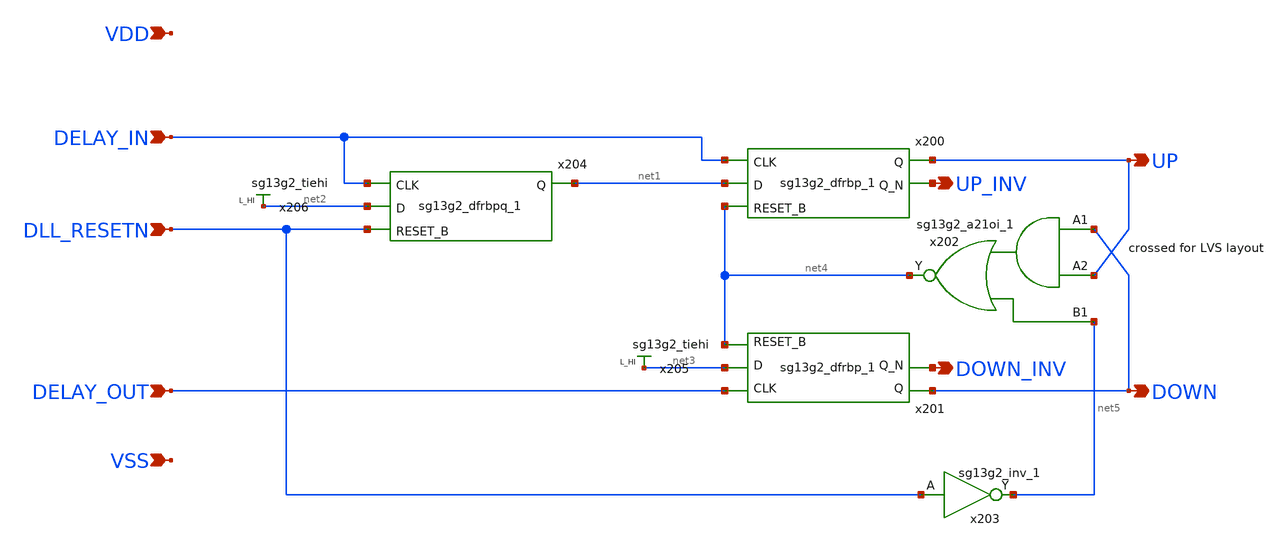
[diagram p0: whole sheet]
** sch_path: schematics/hx_phase_detector.sch
**.subckt hx_phase_detector VDD VSS UP DOWN UP_INV DLL_RESETN DOWN_INV DELAY_IN DELAY_OUT
*.ipin VDD
*.ipin VSS
*.opin UP
*.opin DOWN
*.opin UP_INV
*.ipin DLL_RESETN
*.opin DOWN_INV
*.ipin DELAY_IN
*.ipin DELAY_OUT
x200 UP UP_INV DELAY_IN net1 net4 VDD VSS sg13g2_dfrbp_1
x201 DOWN DOWN_INV DELAY_OUT net3 net4 VDD VSS sg13g2_dfrbp_1
x206 net2 VDD VSS sg13g2_tiehi
x204 net1 DELAY_IN net2 DLL_RESETN VDD VSS sg13g2_dfrbpq_1
x205 net3 VDD VSS sg13g2_tiehi
x202 net4 DOWN UP net5 VDD VSS sg13g2_a21oi_1
x203 net5 DLL_RESETN VDD VSS sg13g2_inv_1
**.ends

* expanding   symbol:  sg13g2_stdcells/sg13g2_dfrbp_1.sym # of pins=5
** sym_path: sg13g2_stdcells/sg13g2_dfrbp_1.sym
** sch_path: sg13g2_stdcells/sg13g2_dfrbp_1.sch
.subckt sg13g2_dfrbp_1 Q Q_N CLK D RESET_B VDD VSS
*.ipin D
*.ipin RESET_B
*.ipin CLK
*.opin Q
*.opin Q_N
*.iopin VDD
*.iopin VSS
XM1 Db D net10 VSS sg13_lv_nmos w=420.00n l=130.00n ng=1 m=1 mm_ok=1
XM2 net10 RESET_B VSS VSS sg13_lv_nmos w=420.00n l=130.00n ng=1 m=1 mm_ok=1
XM3 net1 clkneg net9 VSS sg13_lv_nmos w=420.00n l=130.00n ng=1 m=1 mm_ok=1
XM4 net9 net1 VSS VSS sg13_lv_nmos w=420.00n l=130.00n ng=1 m=1 mm_ok=1
XM5 net1 net1 net5 VSS sg13_lv_nmos w=420.00n l=130.00n ng=1 m=1 mm_ok=1
XM6 net5 RESET_B VSS VSS sg13_lv_nmos w=420.00n l=130.00n ng=1 m=1 mm_ok=1
XM7 Q_N net1 VSS VSS sg13_lv_nmos w=740.00n l=130.00n ng=1 m=1 mm_ok=1
XM8 net2 net1 VSS VSS sg13_lv_nmos w=740.00n l=130.00n ng=1 m=1 mm_ok=1
XM9 Q net2 VSS VSS sg13_lv_nmos w=740.00n l=130.00n ng=1 m=1 mm_ok=1
XM10 clkneg CLK VSS VSS sg13_lv_nmos w=740.00n l=130.00n ng=1 m=1 mm_ok=1
XM11 clkpos clkneg VSS VSS sg13_lv_nmos w=740.00n l=130.00n ng=1 m=1 mm_ok=1
XM12 Db clkneg net3 VSS sg13_lv_nmos w=420.00n l=130.00n ng=1 m=1 mm_ok=1
XM13 net3 clkpos net8 VSS sg13_lv_nmos w=420.00n l=130.00n ng=1 m=1 mm_ok=1
XM14 net8 net3 net4 VSS sg13_lv_nmos w=420.00n l=130.00n ng=1 m=1 mm_ok=1
XM15 net4 RESET_B VSS VSS sg13_lv_nmos w=420.00n l=130.00n ng=1 m=1 mm_ok=1
XM16 net3 net3 VSS VSS sg13_lv_nmos w=740.00n l=130.00n ng=1 m=1 mm_ok=1
XM17 net3 clkpos net1 VSS sg13_lv_nmos w=740.00n l=130.00n ng=1 m=1 mm_ok=1
XM18 Db RESET_B VDD VDD sg13_lv_pmos w=420.00n l=130.00n ng=1 m=1 mm_ok=1
XM19 Db D VDD VDD sg13_lv_pmos w=420.00n l=130.00n ng=1 m=1 mm_ok=1
XM20 net7 net1 VDD VDD sg13_lv_pmos w=420.00n l=130.00n ng=1 m=1 mm_ok=1
XM21 net1 clkpos net7 VDD sg13_lv_pmos w=420.00n l=130.00n ng=1 m=1 mm_ok=1
XM22 net1 net1 VDD VDD sg13_lv_pmos w=420.00n l=130.00n ng=1 m=1 mm_ok=1
XM23 net1 RESET_B VDD VDD sg13_lv_pmos w=420.00n l=130.00n ng=1 m=1 mm_ok=1
XM24 Q_N net1 VDD VDD sg13_lv_pmos w=1.12u l=130.00n ng=1 m=1 mm_ok=1
XM25 net2 net1 VDD VDD sg13_lv_pmos w=1.12u l=130.00n ng=1 m=1 mm_ok=1
XM26 Q net2 VDD VDD sg13_lv_pmos w=1.12u l=130.00n ng=1 m=1 mm_ok=1
XM27 clkneg CLK VDD VDD sg13_lv_pmos w=1.12u l=130.00n ng=1 m=1 mm_ok=1
XM28 clkpos clkneg VDD VDD sg13_lv_pmos w=1.12u l=130.00n ng=1 m=1 mm_ok=1
XM29 Db clkpos net3 VDD sg13_lv_pmos w=420.00n l=130.00n ng=1 m=1 mm_ok=1
XM30 net6 net3 VDD VDD sg13_lv_pmos w=420.00n l=130.00n ng=1 m=1 mm_ok=1
XM31 net3 clkneg net6 VDD sg13_lv_pmos w=420.00n l=130.00n ng=1 m=1 mm_ok=1
XM32 net3 RESET_B VDD VDD sg13_lv_pmos w=420.00n l=130.00n ng=1 m=1 mm_ok=1
XM33 net3 net3 VDD VDD sg13_lv_pmos w=1.000u l=130.00n ng=1 m=1 mm_ok=1
XM34 net3 clkneg net1 VDD sg13_lv_pmos w=1.000u l=130.00n ng=1 m=1 mm_ok=1
.ends


* expanding   symbol:  sg13g2_stdcells/sg13g2_dfrbpq_1.sym # of pins=4
** sym_path: sg13g2_stdcells/sg13g2_dfrbpq_1.sym
** sch_path: sg13g2_stdcells/sg13g2_dfrbpq_1.sch
.subckt sg13g2_dfrbpq_1 Q CLK D RESET_B VDD VSS
*.opin Q
*.ipin CLK
*.ipin D
*.ipin RESET_B
*.iopin VDD
*.iopin VSS
XM1 Db D net10 VSS sg13_lv_nmos w=420.00n l=130.00n ng=1 m=1 mm_ok=1
XM2 net10 RESET_B VSS VSS sg13_lv_nmos w=420.00n l=130.00n ng=1 m=1 mm_ok=1
XM3 net1 clkneg net9 VSS sg13_lv_nmos w=420.00n l=130.00n ng=1 m=1 mm_ok=1
XM4 net9 net1 VSS VSS sg13_lv_nmos w=420.00n l=130.00n ng=1 m=1 mm_ok=1
XM5 net1 net1 net5 VSS sg13_lv_nmos w=420.00n l=130.00n ng=1 m=1 mm_ok=1
XM6 net5 RESET_B VSS VSS sg13_lv_nmos w=420.00n l=130.00n ng=1 m=1 mm_ok=1
XM7 net2 net1 VSS VSS sg13_lv_nmos w=740.00n l=130.00n ng=1 m=1 mm_ok=1
XM8 Q net2 VSS VSS sg13_lv_nmos w=740.00n l=130.00n ng=1 m=1 mm_ok=1
XM9 clkneg CLK VSS VSS sg13_lv_nmos w=740.00n l=130.00n ng=1 m=1 mm_ok=1
XM10 clkpos clkneg VSS VSS sg13_lv_nmos w=740.00n l=130.00n ng=1 m=1 mm_ok=1
XM11 Db clkneg net3 VSS sg13_lv_nmos w=420.00n l=130.00n ng=1 m=1 mm_ok=1
XM12 net3 clkpos net8 VSS sg13_lv_nmos w=420.00n l=130.00n ng=1 m=1 mm_ok=1
XM13 net8 net3 net4 VSS sg13_lv_nmos w=420.00n l=130.00n ng=1 m=1 mm_ok=1
XM14 net4 RESET_B VSS VSS sg13_lv_nmos w=420.00n l=130.00n ng=1 m=1 mm_ok=1
XM15 net3 net3 VSS VSS sg13_lv_nmos w=740.00n l=130.00n ng=1 m=1 mm_ok=1
XM16 net3 clkpos net1 VSS sg13_lv_nmos w=740.00n l=130.00n ng=1 m=1 mm_ok=1
XM17 Db RESET_B VDD VDD sg13_lv_pmos w=420.00n l=130.00n ng=1 m=1 mm_ok=1
XM18 Db D VDD VDD sg13_lv_pmos w=420.00n l=130.00n ng=1 m=1 mm_ok=1
XM19 net7 net1 VDD VDD sg13_lv_pmos w=420.00n l=130.00n ng=1 m=1 mm_ok=1
XM20 net1 clkpos net7 VDD sg13_lv_pmos w=420.00n l=130.00n ng=1 m=1 mm_ok=1
XM21 net1 net1 VDD VDD sg13_lv_pmos w=420.00n l=130.00n ng=1 m=1 mm_ok=1
XM22 net1 RESET_B VDD VDD sg13_lv_pmos w=420.00n l=130.00n ng=1 m=1 mm_ok=1
XM23 net2 net1 VDD VDD sg13_lv_pmos w=1.12u l=130.00n ng=1 m=1 mm_ok=1
XM24 Q net2 VDD VDD sg13_lv_pmos w=1.12u l=130.00n ng=1 m=1 mm_ok=1
XM25 clkneg CLK VDD VDD sg13_lv_pmos w=1.12u l=130.00n ng=1 m=1 mm_ok=1
XM26 clkpos clkneg VDD VDD sg13_lv_pmos w=1.12u l=130.00n ng=1 m=1 mm_ok=1
XM27 Db clkpos net3 VDD sg13_lv_pmos w=420.00n l=130.00n ng=1 m=1 mm_ok=1
XM28 net6 net3 VDD VDD sg13_lv_pmos w=420.00n l=130.00n ng=1 m=1 mm_ok=1
XM29 net3 clkneg net6 VDD sg13_lv_pmos w=420.00n l=130.00n ng=1 m=1 mm_ok=1
XM30 net3 RESET_B VDD VDD sg13_lv_pmos w=420.00n l=130.00n ng=1 m=1 mm_ok=1
XM31 net3 net3 VDD VDD sg13_lv_pmos w=1.000u l=130.00n ng=1 m=1 mm_ok=1
XM32 net3 clkneg net1 VDD sg13_lv_pmos w=1.000u l=130.00n ng=1 m=1 mm_ok=1
.ends


* expanding   symbol:  sg13g2_a21oi_1.sym # of pins=4
** sym_path: sg13g2_a21oi_1.sym
** sch_path: sg13g2_a21oi_1.sch
.subckt sg13g2_a21oi_1 Y A1 A2 B1 VDD VSS
*.ipin A1
*.ipin A2
*.ipin B1
*.opin Y
*.iopin VDD
*.iopin VSS
XM1 Y B1 VSS VSS sg13_lv_nmos w=740.00n l=130.00n ng=1 m=1 mm_ok=1
XM2 Y A1 net2 VSS sg13_lv_nmos w=740.00n l=130.00n ng=1 m=1 mm_ok=1
XM3 net2 A2 VSS VSS sg13_lv_nmos w=740.00n l=130.00n ng=1 m=1 mm_ok=1
XM4 net1 A1 VDD VDD sg13_lv_pmos w=1.12u l=130.00n ng=1 m=1 mm_ok=1
XM5 net1 A2 VDD VDD sg13_lv_pmos w=1.12u l=130.00n ng=1 m=1 mm_ok=1
XM6 Y B1 net1 VDD sg13_lv_pmos w=1.12u l=130.00n ng=1 m=1 mm_ok=1
.ends


* expanding   symbol:  sg13g2_inv_1.sym # of pins=2
** sym_path: sg13g2_inv_1.sym
** sch_path: sg13g2_inv_1.sch
.subckt sg13g2_inv_1 Y A VDD VSS
*.opin Y
*.ipin A
*.iopin VDD
*.iopin VSS
XM1 Y A VSS VSS sg13_lv_nmos w=740.00n l=130.00n ng=1 m=1 mm_ok=1
XM2 Y A VDD VDD sg13_lv_pmos w=1.12u l=130.00n ng=1 m=1 mm_ok=1
.ends

.end
